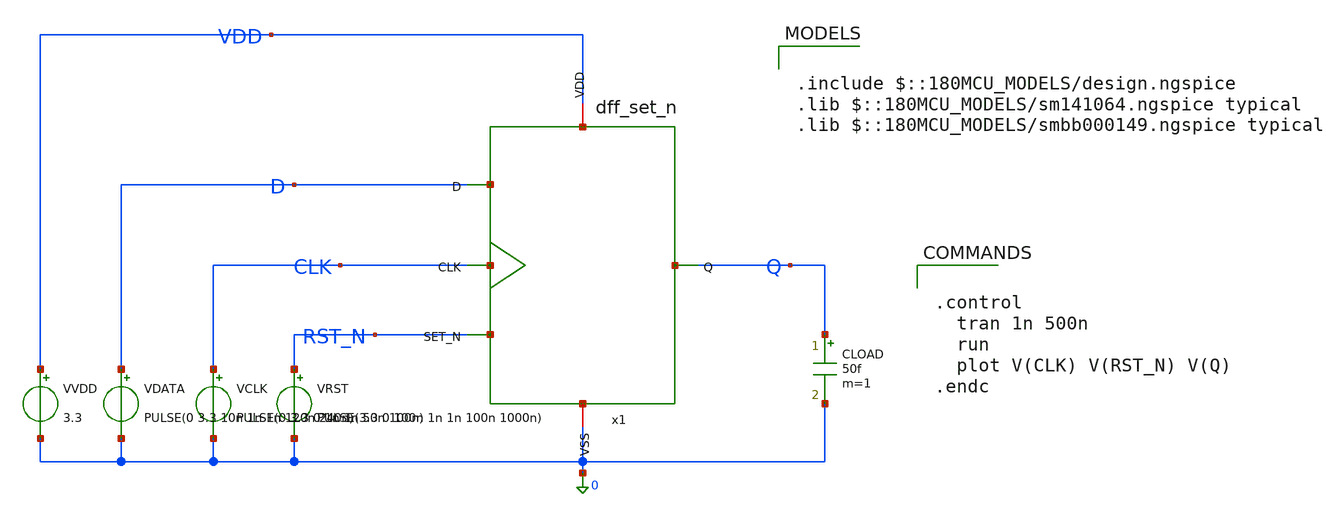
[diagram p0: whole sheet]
** sch_path: sar_logic/sar_designs/tb_dff_set_n.sch
**.subckt tb_dff_set_n
VRST RST_N 0 PULSE(3.3 0 100n 1n 1n 100n 1000n)
VCLK CLK 0 PULSE(0 3.3 0 1n 1n 50n 100n)
VDATA D 0 PULSE(0 3.3 10n 1n 1n 120n 240n)
VVDD VDD 0 3.3
CLOAD Q 0 50f m=1
x1 VDD CLK D Q RST_N 0 dff_set_n
**** begin user architecture code

.include $::180MCU_MODELS/design.ngspice
.lib $::180MCU_MODELS/sm141064.ngspice typical
.lib $::180MCU_MODELS/smbb000149.ngspice typical



.control
  tran 1n 500n
  run
  plot V(CLK) V(RST_N) V(Q)
.endc


**** end user architecture code
**.ends
.end
